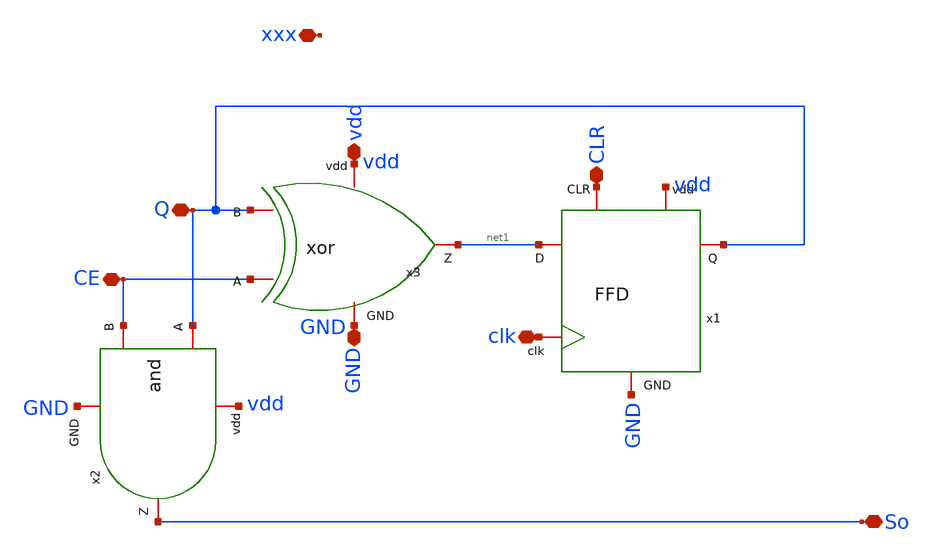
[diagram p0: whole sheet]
** sch_path: simbolos y esquematicos/untitled.sch
**.subckt untitled Q xxx CLR clk So CE GND vdd
*.iopin Q
*.iopin xxx
*.iopin CLR
*.iopin clk
*.iopin So
*.iopin CE
*.iopin GND
*.iopin vdd
x1 vdd GND CLR Q net1 clk FFD
x2 vdd Q So CE GND and
x3 vdd CE Q net1 GND xor
**.ends
.end
